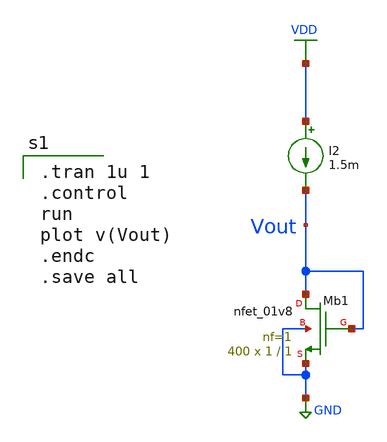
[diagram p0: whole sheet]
** sch_path: Circuits/Examples/Analog/Trans_Testing/NMOS_Test.sch
**.subckt NMOS_Test
XMb1 Vout Vout GND GND sky130_fd_pr__nfet_01v8 L=1 W=1 nf=1 ad='int((nf+1)/2) * W/nf * 0.29' as='int((nf+2)/2) * W/nf * 0.29'
+ pd='2*int((nf+1)/2) * (W/nf + 0.29)' ps='2*int((nf+2)/2) * (W/nf + 0.29)' nrd='0.29 / W' nrs='0.29 / W'
+ sa=0 sb=0 sd=0 mult=400 m=400
I2 VDD Vout 1.5m
**** begin user architecture code
 ** manual skywater pdks install (with patches applied)
* .lib $::SKYWATER_MODELS/models/sky130.lib.spice tt

** opencircuitdesign pdks install
.lib $::SKYWATER_MODELS/sky130.lib.spice tt

.param mc_mm_switch=0
.param mc_pr_switch=0


.tran 1u 1
.control
run
plot v(Vout)
.endc
.save all

**** end user architecture code
**.ends
.GLOBAL GND
.GLOBAL VDD
.end
